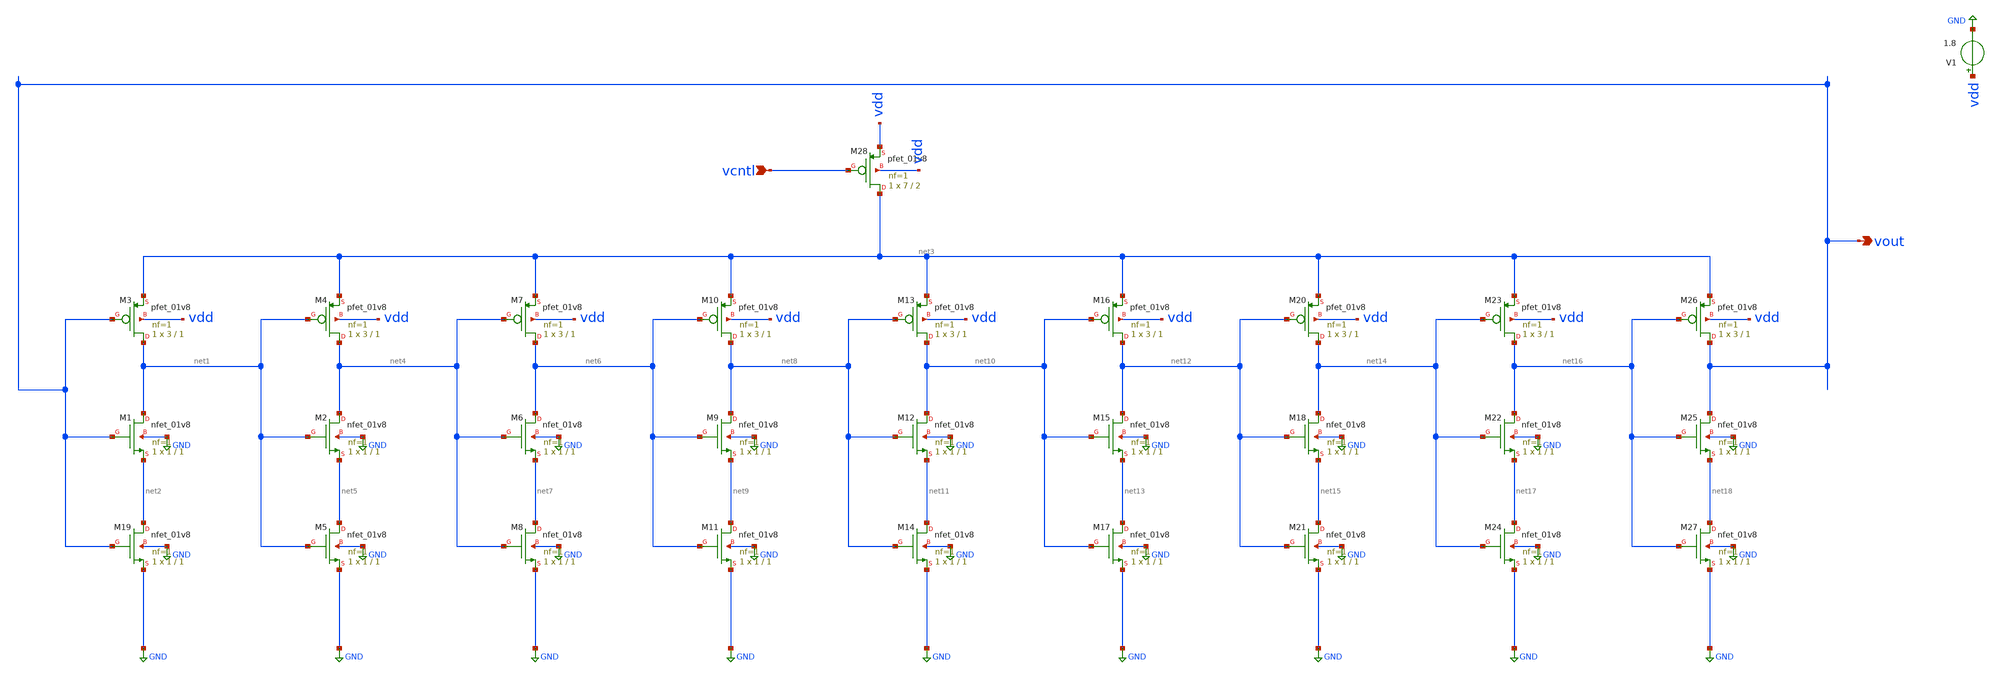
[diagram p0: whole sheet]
** sch_path: osci.sch
**.subckt osci vcntl vout
*.ipin vcntl
*.opin vout
XM1 net1 vout net2 GND sky130_fd_pr__nfet_01v8 L=1 W=1 nf=1 ad='int((nf+1)/2) * W/nf * 0.29' as='int((nf+2)/2) * W/nf * 0.29'
+ pd='2*int((nf+1)/2) * (W/nf + 0.29)' ps='2*int((nf+2)/2) * (W/nf + 0.29)' nrd='0.29 / W' nrs='0.29 / W'
+ sa=0 sb=0 sd=0 mult=1 m=1
XM3 net1 vout net3 vdd sky130_fd_pr__pfet_01v8 L=1 W=3 nf=1 ad='int((nf+1)/2) * W/nf * 0.29' as='int((nf+2)/2) * W/nf * 0.29'
+ pd='2*int((nf+1)/2) * (W/nf + 0.29)' ps='2*int((nf+2)/2) * (W/nf + 0.29)' nrd='0.29 / W' nrs='0.29 / W'
+ sa=0 sb=0 sd=0 mult=1 m=1
XM19 net2 vout GND GND sky130_fd_pr__nfet_01v8 L=1 W=1 nf=1 ad='int((nf+1)/2) * W/nf * 0.29' as='int((nf+2)/2) * W/nf * 0.29'
+ pd='2*int((nf+1)/2) * (W/nf + 0.29)' ps='2*int((nf+2)/2) * (W/nf + 0.29)' nrd='0.29 / W' nrs='0.29 / W'
+ sa=0 sb=0 sd=0 mult=1 m=1
V1 vdd GND 1.8
XM28 net3 vcntl vdd vdd sky130_fd_pr__pfet_01v8 L=2 W=7 nf=1 ad='int((nf+1)/2) * W/nf * 0.29' as='int((nf+2)/2) * W/nf * 0.29'
+ pd='2*int((nf+1)/2) * (W/nf + 0.29)' ps='2*int((nf+2)/2) * (W/nf + 0.29)' nrd='0.29 / W' nrs='0.29 / W'
+ sa=0 sb=0 sd=0 mult=1 m=1
XM2 net4 net1 net5 GND sky130_fd_pr__nfet_01v8 L=1 W=1 nf=1 ad='int((nf+1)/2) * W/nf * 0.29' as='int((nf+2)/2) * W/nf * 0.29'
+ pd='2*int((nf+1)/2) * (W/nf + 0.29)' ps='2*int((nf+2)/2) * (W/nf + 0.29)' nrd='0.29 / W' nrs='0.29 / W'
+ sa=0 sb=0 sd=0 mult=1 m=1
XM4 net4 net1 net3 vdd sky130_fd_pr__pfet_01v8 L=1 W=3 nf=1 ad='int((nf+1)/2) * W/nf * 0.29' as='int((nf+2)/2) * W/nf * 0.29'
+ pd='2*int((nf+1)/2) * (W/nf + 0.29)' ps='2*int((nf+2)/2) * (W/nf + 0.29)' nrd='0.29 / W' nrs='0.29 / W'
+ sa=0 sb=0 sd=0 mult=1 m=1
XM5 net5 net1 GND GND sky130_fd_pr__nfet_01v8 L=1 W=1 nf=1 ad='int((nf+1)/2) * W/nf * 0.29' as='int((nf+2)/2) * W/nf * 0.29'
+ pd='2*int((nf+1)/2) * (W/nf + 0.29)' ps='2*int((nf+2)/2) * (W/nf + 0.29)' nrd='0.29 / W' nrs='0.29 / W'
+ sa=0 sb=0 sd=0 mult=1 m=1
XM6 net6 net4 net7 GND sky130_fd_pr__nfet_01v8 L=1 W=1 nf=1 ad='int((nf+1)/2) * W/nf * 0.29' as='int((nf+2)/2) * W/nf * 0.29'
+ pd='2*int((nf+1)/2) * (W/nf + 0.29)' ps='2*int((nf+2)/2) * (W/nf + 0.29)' nrd='0.29 / W' nrs='0.29 / W'
+ sa=0 sb=0 sd=0 mult=1 m=1
XM7 net6 net4 net3 vdd sky130_fd_pr__pfet_01v8 L=1 W=3 nf=1 ad='int((nf+1)/2) * W/nf * 0.29' as='int((nf+2)/2) * W/nf * 0.29'
+ pd='2*int((nf+1)/2) * (W/nf + 0.29)' ps='2*int((nf+2)/2) * (W/nf + 0.29)' nrd='0.29 / W' nrs='0.29 / W'
+ sa=0 sb=0 sd=0 mult=1 m=1
XM8 net7 net4 GND GND sky130_fd_pr__nfet_01v8 L=1 W=1 nf=1 ad='int((nf+1)/2) * W/nf * 0.29' as='int((nf+2)/2) * W/nf * 0.29'
+ pd='2*int((nf+1)/2) * (W/nf + 0.29)' ps='2*int((nf+2)/2) * (W/nf + 0.29)' nrd='0.29 / W' nrs='0.29 / W'
+ sa=0 sb=0 sd=0 mult=1 m=1
XM9 net8 net6 net9 GND sky130_fd_pr__nfet_01v8 L=1 W=1 nf=1 ad='int((nf+1)/2) * W/nf * 0.29' as='int((nf+2)/2) * W/nf * 0.29'
+ pd='2*int((nf+1)/2) * (W/nf + 0.29)' ps='2*int((nf+2)/2) * (W/nf + 0.29)' nrd='0.29 / W' nrs='0.29 / W'
+ sa=0 sb=0 sd=0 mult=1 m=1
XM10 net8 net6 net3 vdd sky130_fd_pr__pfet_01v8 L=1 W=3 nf=1 ad='int((nf+1)/2) * W/nf * 0.29' as='int((nf+2)/2) * W/nf * 0.29'
+ pd='2*int((nf+1)/2) * (W/nf + 0.29)' ps='2*int((nf+2)/2) * (W/nf + 0.29)' nrd='0.29 / W' nrs='0.29 / W'
+ sa=0 sb=0 sd=0 mult=1 m=1
XM11 net9 net6 GND GND sky130_fd_pr__nfet_01v8 L=1 W=1 nf=1 ad='int((nf+1)/2) * W/nf * 0.29' as='int((nf+2)/2) * W/nf * 0.29'
+ pd='2*int((nf+1)/2) * (W/nf + 0.29)' ps='2*int((nf+2)/2) * (W/nf + 0.29)' nrd='0.29 / W' nrs='0.29 / W'
+ sa=0 sb=0 sd=0 mult=1 m=1
XM12 net10 net8 net11 GND sky130_fd_pr__nfet_01v8 L=1 W=1 nf=1 ad='int((nf+1)/2) * W/nf * 0.29' as='int((nf+2)/2) * W/nf * 0.29'
+ pd='2*int((nf+1)/2) * (W/nf + 0.29)' ps='2*int((nf+2)/2) * (W/nf + 0.29)' nrd='0.29 / W' nrs='0.29 / W'
+ sa=0 sb=0 sd=0 mult=1 m=1
XM13 net10 net8 net3 vdd sky130_fd_pr__pfet_01v8 L=1 W=3 nf=1 ad='int((nf+1)/2) * W/nf * 0.29' as='int((nf+2)/2) * W/nf * 0.29'
+ pd='2*int((nf+1)/2) * (W/nf + 0.29)' ps='2*int((nf+2)/2) * (W/nf + 0.29)' nrd='0.29 / W' nrs='0.29 / W'
+ sa=0 sb=0 sd=0 mult=1 m=1
XM14 net11 net8 GND GND sky130_fd_pr__nfet_01v8 L=1 W=1 nf=1 ad='int((nf+1)/2) * W/nf * 0.29' as='int((nf+2)/2) * W/nf * 0.29'
+ pd='2*int((nf+1)/2) * (W/nf + 0.29)' ps='2*int((nf+2)/2) * (W/nf + 0.29)' nrd='0.29 / W' nrs='0.29 / W'
+ sa=0 sb=0 sd=0 mult=1 m=1
XM15 net12 net10 net13 GND sky130_fd_pr__nfet_01v8 L=1 W=1 nf=1 ad='int((nf+1)/2) * W/nf * 0.29' as='int((nf+2)/2) * W/nf * 0.29'
+ pd='2*int((nf+1)/2) * (W/nf + 0.29)' ps='2*int((nf+2)/2) * (W/nf + 0.29)' nrd='0.29 / W' nrs='0.29 / W'
+ sa=0 sb=0 sd=0 mult=1 m=1
XM16 net12 net10 net3 vdd sky130_fd_pr__pfet_01v8 L=1 W=3 nf=1 ad='int((nf+1)/2) * W/nf * 0.29' as='int((nf+2)/2) * W/nf * 0.29'
+ pd='2*int((nf+1)/2) * (W/nf + 0.29)' ps='2*int((nf+2)/2) * (W/nf + 0.29)' nrd='0.29 / W' nrs='0.29 / W'
+ sa=0 sb=0 sd=0 mult=1 m=1
XM17 net13 net10 GND GND sky130_fd_pr__nfet_01v8 L=1 W=1 nf=1 ad='int((nf+1)/2) * W/nf * 0.29' as='int((nf+2)/2) * W/nf * 0.29'
+ pd='2*int((nf+1)/2) * (W/nf + 0.29)' ps='2*int((nf+2)/2) * (W/nf + 0.29)' nrd='0.29 / W' nrs='0.29 / W'
+ sa=0 sb=0 sd=0 mult=1 m=1
XM18 net14 net12 net15 GND sky130_fd_pr__nfet_01v8 L=1 W=1 nf=1 ad='int((nf+1)/2) * W/nf * 0.29' as='int((nf+2)/2) * W/nf * 0.29'
+ pd='2*int((nf+1)/2) * (W/nf + 0.29)' ps='2*int((nf+2)/2) * (W/nf + 0.29)' nrd='0.29 / W' nrs='0.29 / W'
+ sa=0 sb=0 sd=0 mult=1 m=1
XM20 net14 net12 net3 vdd sky130_fd_pr__pfet_01v8 L=1 W=3 nf=1 ad='int((nf+1)/2) * W/nf * 0.29' as='int((nf+2)/2) * W/nf * 0.29'
+ pd='2*int((nf+1)/2) * (W/nf + 0.29)' ps='2*int((nf+2)/2) * (W/nf + 0.29)' nrd='0.29 / W' nrs='0.29 / W'
+ sa=0 sb=0 sd=0 mult=1 m=1
XM21 net15 net12 GND GND sky130_fd_pr__nfet_01v8 L=1 W=1 nf=1 ad='int((nf+1)/2) * W/nf * 0.29' as='int((nf+2)/2) * W/nf * 0.29'
+ pd='2*int((nf+1)/2) * (W/nf + 0.29)' ps='2*int((nf+2)/2) * (W/nf + 0.29)' nrd='0.29 / W' nrs='0.29 / W'
+ sa=0 sb=0 sd=0 mult=1 m=1
XM22 net16 net14 net17 GND sky130_fd_pr__nfet_01v8 L=1 W=1 nf=1 ad='int((nf+1)/2) * W/nf * 0.29' as='int((nf+2)/2) * W/nf * 0.29'
+ pd='2*int((nf+1)/2) * (W/nf + 0.29)' ps='2*int((nf+2)/2) * (W/nf + 0.29)' nrd='0.29 / W' nrs='0.29 / W'
+ sa=0 sb=0 sd=0 mult=1 m=1
XM23 net16 net14 net3 vdd sky130_fd_pr__pfet_01v8 L=1 W=3 nf=1 ad='int((nf+1)/2) * W/nf * 0.29' as='int((nf+2)/2) * W/nf * 0.29'
+ pd='2*int((nf+1)/2) * (W/nf + 0.29)' ps='2*int((nf+2)/2) * (W/nf + 0.29)' nrd='0.29 / W' nrs='0.29 / W'
+ sa=0 sb=0 sd=0 mult=1 m=1
XM24 net17 net14 GND GND sky130_fd_pr__nfet_01v8 L=1 W=1 nf=1 ad='int((nf+1)/2) * W/nf * 0.29' as='int((nf+2)/2) * W/nf * 0.29'
+ pd='2*int((nf+1)/2) * (W/nf + 0.29)' ps='2*int((nf+2)/2) * (W/nf + 0.29)' nrd='0.29 / W' nrs='0.29 / W'
+ sa=0 sb=0 sd=0 mult=1 m=1
XM25 vout net16 net18 GND sky130_fd_pr__nfet_01v8 L=1 W=1 nf=1 ad='int((nf+1)/2) * W/nf * 0.29' as='int((nf+2)/2) * W/nf * 0.29'
+ pd='2*int((nf+1)/2) * (W/nf + 0.29)' ps='2*int((nf+2)/2) * (W/nf + 0.29)' nrd='0.29 / W' nrs='0.29 / W'
+ sa=0 sb=0 sd=0 mult=1 m=1
XM26 vout net16 net3 vdd sky130_fd_pr__pfet_01v8 L=1 W=3 nf=1 ad='int((nf+1)/2) * W/nf * 0.29' as='int((nf+2)/2) * W/nf * 0.29'
+ pd='2*int((nf+1)/2) * (W/nf + 0.29)' ps='2*int((nf+2)/2) * (W/nf + 0.29)' nrd='0.29 / W' nrs='0.29 / W'
+ sa=0 sb=0 sd=0 mult=1 m=1
XM27 net18 net16 GND GND sky130_fd_pr__nfet_01v8 L=1 W=1 nf=1 ad='int((nf+1)/2) * W/nf * 0.29' as='int((nf+2)/2) * W/nf * 0.29'
+ pd='2*int((nf+1)/2) * (W/nf + 0.29)' ps='2*int((nf+2)/2) * (W/nf + 0.29)' nrd='0.29 / W' nrs='0.29 / W'
+ sa=0 sb=0 sd=0 mult=1 m=1
**.ends
.GLOBAL GND
.end
